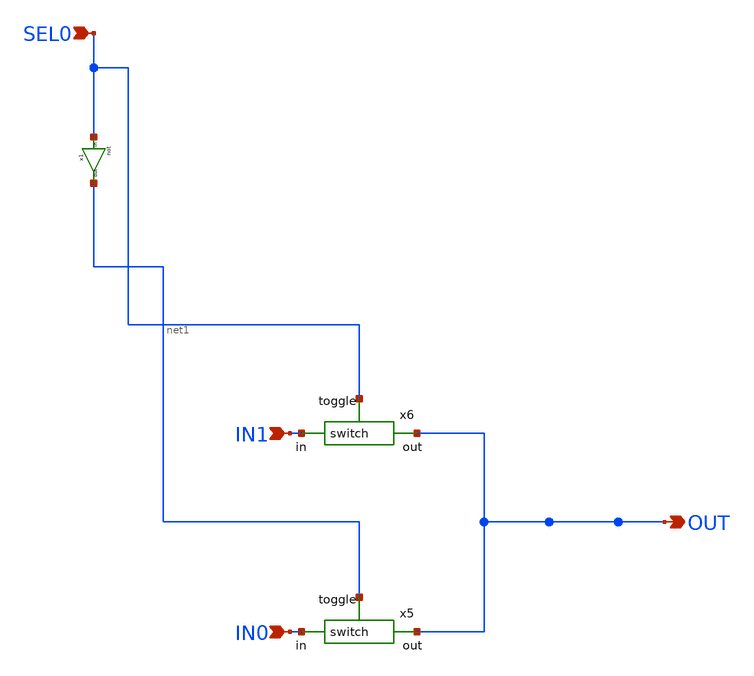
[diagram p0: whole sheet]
** sch_path: xschem/mux2_1/mux2_1.sch
**.subckt mux2_1 SEL0 OUT IN1 IN0
*.ipin SEL0
*.opin OUT
*.ipin IN1
*.ipin IN0
x1 net1 SEL0 not
x6 SEL0 OUT IN1 switch
x5 net1 OUT IN0 switch
**.ends

* expanding   symbol:  not/not.sym # of pins=2
** sym_path: xschem/not/not.sym
** sch_path: xschem/not/not.sch
.subckt not out in
*.ipin in
*.opin out
XM10 out in VDD VDD sky130_fd_pr__pfet_01v8_lvt L=0.35 W=1 nf=1 ad='int((1 + 1)/2) * 1 / 1 * 0.29' as='int((1 + 2)/2) * 1 / 1 * 0.29'
+ pd='2*int((1 + 1)/2) * (1 / 1 + 0.29)' ps='2*int((1 + 2)/2) * (1 / 1 + 0.29)' nrd='0.29 / 1 ' nrs='0.29 / 1 '
+ sa=0 sb=0 sd=0 mult=1 m=1
XM1 out in GND GND sky130_fd_pr__nfet_01v8_lvt L=0.15 W=1 nf=1 ad='int((1 + 1)/2) * 1 / 1 * 0.29' as='int((1 + 2)/2) * 1 / 1 * 0.29'
+ pd='2*int((1 + 1)/2) * (1 / 1 + 0.29)' ps='2*int((1 + 2)/2) * (1 / 1 + 0.29)' nrd='0.29 / 1 ' nrs='0.29 / 1 '
+ sa=0 sb=0 sd=0 mult=1 m=1
.ends


* expanding   symbol:  switch/switch.sym # of pins=3
** sym_path: xschem/switch/switch.sym
** sch_path: xschem/switch/switch.sch
.subckt switch toggle out in
*.ipin toggle
*.ipin in
*.opin out
x1 net1 toggle not
XM26 out net1 in VDD sky130_fd_pr__pfet_01v8_lvt L=3 W=200 nf=5 ad='int((5 + 1)/2) * 200 / 5 * 0.29'
+ as='int((5 + 2)/2) * 200 / 5 * 0.29' pd='2*int((5 + 1)/2) * (200 / 5 + 0.29)' ps='2*int((5 + 2)/2) * (200 / 5 + 0.29)'
+ nrd='0.29 / 200 ' nrs='0.29 / 200 ' sa=0 sb=0 sd=0 mult=1 m=1
XM17 in toggle out GND sky130_fd_pr__nfet_01v8_lvt L=3 W=200 nf=5 ad='int((5 + 1)/2) * 200 / 5 * 0.29'
+ as='int((5 + 2)/2) * 200 / 5 * 0.29' pd='2*int((5 + 1)/2) * (200 / 5 + 0.29)' ps='2*int((5 + 2)/2) * (200 / 5 + 0.29)'
+ nrd='0.29 / 200 ' nrs='0.29 / 200 ' sa=0 sb=0 sd=0 mult=1 m=1
.ends

.GLOBAL VDD
.GLOBAL GND
.end
